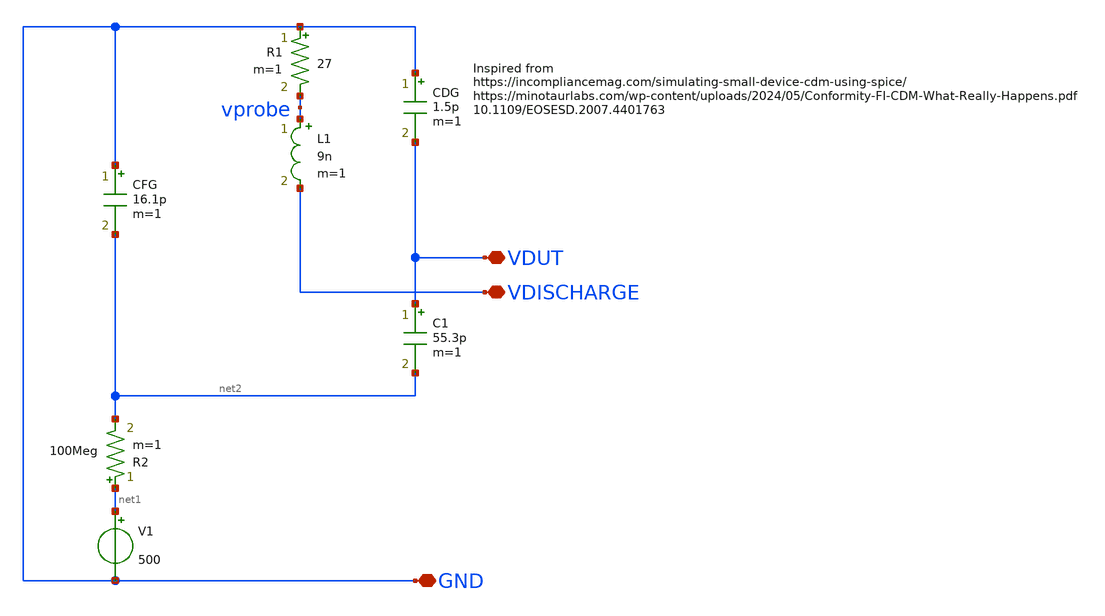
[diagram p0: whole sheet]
** sch_path: gf180mcuD/xschem-simul/cdm_tester.sch
**.subckt cdm_tester VDUT GND VDISCHARGE
*.iopin VDUT
*.iopin GND
*.iopin VDISCHARGE
L1 vprobe VDISCHARGE 9n m=1
R1 GND vprobe 27 m=1
CDG GND VDUT 1.5p m=1
CFG GND net2 16.1p m=1
R2 net1 net2 100Meg m=1
V1 net1 GND 500
C1 VDUT net2 55.3p m=1
**.ends
.end
